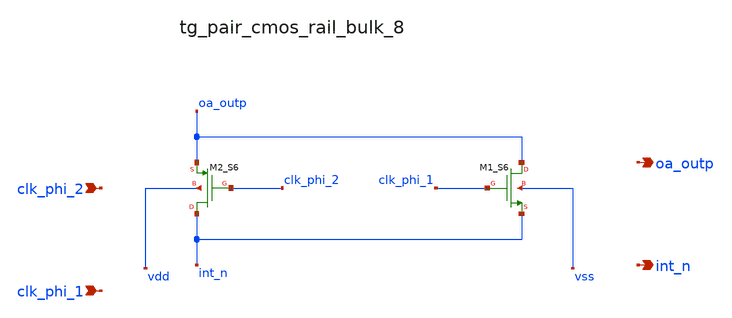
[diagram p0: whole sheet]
** sch_path: analog-db/raw/sup_003_rrl_sc_integrator/hier/blocks/tg_pair_cmos_rail_bulk_8.sch
**.subckt tg_pair_cmos_rail_bulk_8 clk_phi_2 clk_phi_1 oa_outp int_n
*.ipin clk_phi_2
*.ipin clk_phi_1
*.opin oa_outp
*.opin int_n
XM1_S6 oa_outp clk_phi_1 int_n vss sg13_lv_nmos w=x_dut_xm1_s6_w l=x_dut_xm1_s6_l ng=1
+ m=x_dut_xm1_s6_m
XM2_S6 int_n clk_phi_2 oa_outp vdd sg13_lv_pmos w=x_dut_xm2_s6_w l=x_dut_xm2_s6_l ng=1
+ m=x_dut_xm2_s6_m
**.ends
.end
